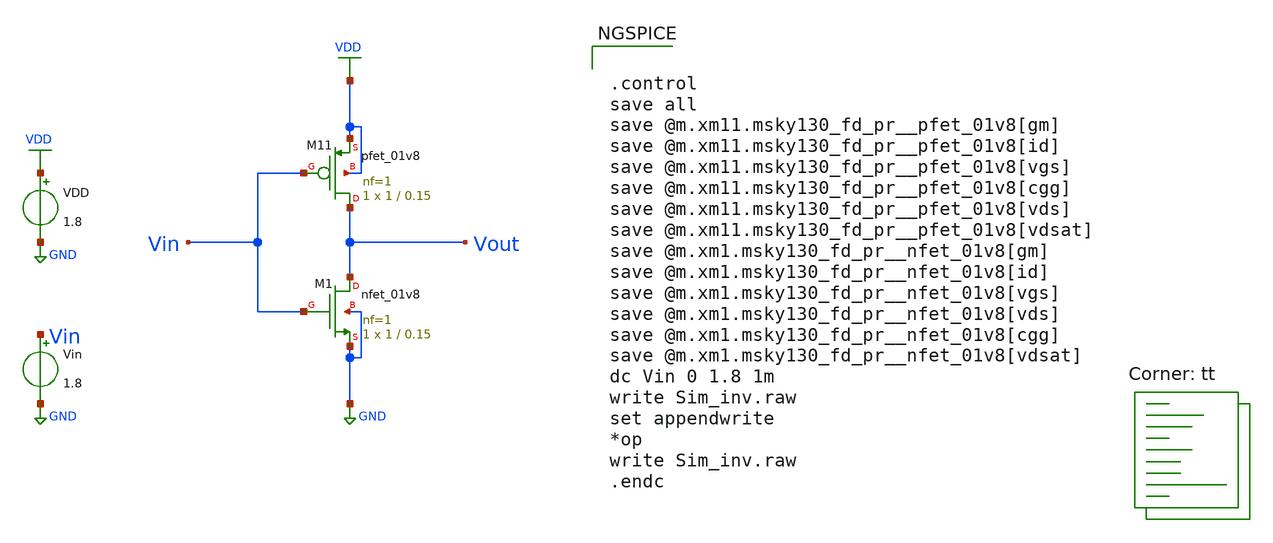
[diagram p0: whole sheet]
** sch_path: Sim_inv.sch
**.subckt Sim_inv
XM1 Vout Vin GND GND sky130_fd_pr__nfet_01v8 L=0.15 W=1 nf=1 ad='int((1 + 1)/2) * 1 / 1 * 0.29' as='int((1 + 2)/2) * 1 / 1 * 0.29'
+ pd='2*int((1 + 1)/2) * (1 / 1 + 0.29)' ps='2*int((1 + 2)/2) * (1 / 1 + 0.29)' nrd='0.29 / 1 ' nrs='0.29 / 1 '
+ sa=0 sb=0 sd=0 mult=1 m=1
XM11 Vout Vin VDD VDD sky130_fd_pr__pfet_01v8 L=0.15 W=1 nf=1 ad='int((nf+1)/2) * W/nf * 0.29' as='int((nf+2)/2) * W/nf * 0.29'
+ pd='2*int((nf+1)/2) * (W/nf + 0.29)' ps='2*int((nf+2)/2) * (W/nf + 0.29)' nrd='0.29 / W' nrs='0.29 / W'
+ sa=0 sb=0 sd=0 mult=1 m=1
VDD VDD GND 1.8
Vin Vin GND 1.8
**** begin user architecture code
.lib $::SKYWATER_MODELS/sky130.lib.spice tt


.control
save all
save @m.xm11.msky130_fd_pr__pfet_01v8[gm]
save @m.xm11.msky130_fd_pr__pfet_01v8[id]
save @m.xm11.msky130_fd_pr__pfet_01v8[vgs]
save @m.xm11.msky130_fd_pr__pfet_01v8[cgg]
save @m.xm11.msky130_fd_pr__pfet_01v8[vds]
save @m.xm11.msky130_fd_pr__pfet_01v8[vdsat]
save @m.xm1.msky130_fd_pr__nfet_01v8[gm]
save @m.xm1.msky130_fd_pr__nfet_01v8[id]
save @m.xm1.msky130_fd_pr__nfet_01v8[vgs]
save @m.xm1.msky130_fd_pr__nfet_01v8[vds]
save @m.xm1.msky130_fd_pr__nfet_01v8[cgg]
save @m.xm1.msky130_fd_pr__nfet_01v8[vdsat]
dc Vin 0 1.8 1m
write Sim_inv.raw
set appendwrite
*op
write Sim_inv.raw
.endc


**** end user architecture code
**.ends
.GLOBAL VDD
.GLOBAL GND
.end
